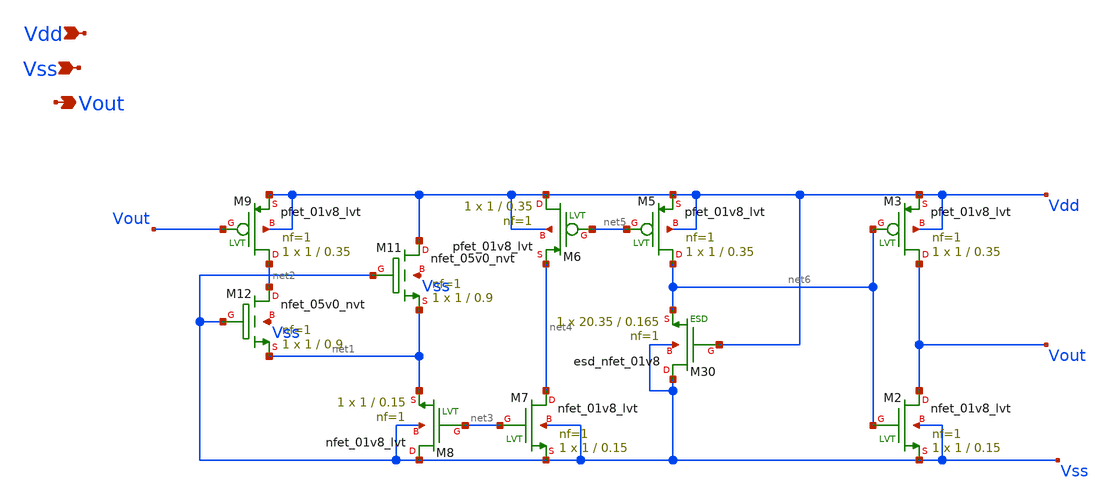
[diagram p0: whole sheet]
** sch_path: tt10-hdl/tt_um_test_commit/xschem/T2/startup/POR/Z_old/native-HengYou_por.sch
**.subckt native-HengYou_por Vdd Vss Vout
*.ipin Vdd
*.ipin Vss
*.opin Vout
XM30 Vss Vdd net6 Vss sky130_fd_pr__esd_nfet_01v8 L=0.165 W=20.35 nf=1 ad='int((nf+1)/2) * W/nf * 0.29'
+ as='int((nf+2)/2) * W/nf * 0.29' pd='2*int((nf+1)/2) * (W/nf + 0.29)' ps='2*int((nf+2)/2) * (W/nf + 0.29)'
+ nrd='0.29 / W' nrs='0.29 / W' sa=0 sb=0 sd=0 mult=1 m=1
XM2 Vout net6 Vss Vss sky130_fd_pr__nfet_01v8_lvt L=0.15 W=1 nf=1 ad='int((1 + 1)/2) * 1 / 1 * 0.29'
+ as='int((1 + 2)/2) * 1 / 1 * 0.29' pd='2*int((1 + 1)/2) * (1 / 1 + 0.29)' ps='2*int((1 + 2)/2) * (1 / 1 + 0.29)'
+ nrd='0.29 / 1 ' nrs='0.29 / 1 ' sa=0 sb=0 sd=0 mult=1 m=1
XM3 Vout net6 Vdd Vdd sky130_fd_pr__pfet_01v8_lvt L=0.35 W=1 nf=1 ad='int((1 + 1)/2) * 1 / 1 * 0.29'
+ as='int((1 + 2)/2) * 1 / 1 * 0.29' pd='2*int((1 + 1)/2) * (1 / 1 + 0.29)' ps='2*int((1 + 2)/2) * (1 / 1 + 0.29)'
+ nrd='0.29 / 1 ' nrs='0.29 / 1 ' sa=0 sb=0 sd=0 mult=1 m=1
XM5 net6 net5 Vdd Vdd sky130_fd_pr__pfet_01v8_lvt L=0.35 W=1 nf=1 ad='int((1 + 1)/2) * 1 / 1 * 0.29'
+ as='int((1 + 2)/2) * 1 / 1 * 0.29' pd='2*int((1 + 1)/2) * (1 / 1 + 0.29)' ps='2*int((1 + 2)/2) * (1 / 1 + 0.29)'
+ nrd='0.29 / 1 ' nrs='0.29 / 1 ' sa=0 sb=0 sd=0 mult=1 m=1
XM6 Vdd net5 net4 Vdd sky130_fd_pr__pfet_01v8_lvt L=0.35 W=1 nf=1 ad='int((1 + 1)/2) * 1 / 1 * 0.29'
+ as='int((1 + 2)/2) * 1 / 1 * 0.29' pd='2*int((1 + 1)/2) * (1 / 1 + 0.29)' ps='2*int((1 + 2)/2) * (1 / 1 + 0.29)'
+ nrd='0.29 / 1 ' nrs='0.29 / 1 ' sa=0 sb=0 sd=0 mult=1 m=1
XM7 net4 net3 Vss Vss sky130_fd_pr__nfet_01v8_lvt L=0.15 W=1 nf=1 ad='int((1 + 1)/2) * 1 / 1 * 0.29'
+ as='int((1 + 2)/2) * 1 / 1 * 0.29' pd='2*int((1 + 1)/2) * (1 / 1 + 0.29)' ps='2*int((1 + 2)/2) * (1 / 1 + 0.29)'
+ nrd='0.29 / 1 ' nrs='0.29 / 1 ' sa=0 sb=0 sd=0 mult=1 m=1
XM8 Vss net3 net1 Vss sky130_fd_pr__nfet_01v8_lvt L=0.15 W=1 nf=1 ad='int((1 + 1)/2) * 1 / 1 * 0.29'
+ as='int((1 + 2)/2) * 1 / 1 * 0.29' pd='2*int((1 + 1)/2) * (1 / 1 + 0.29)' ps='2*int((1 + 2)/2) * (1 / 1 + 0.29)'
+ nrd='0.29 / 1 ' nrs='0.29 / 1 ' sa=0 sb=0 sd=0 mult=1 m=1
XM9 net2 Vout Vdd Vdd sky130_fd_pr__pfet_01v8_lvt L=0.35 W=1 nf=1 ad='int((1 + 1)/2) * 1 / 1 * 0.29'
+ as='int((1 + 2)/2) * 1 / 1 * 0.29' pd='2*int((1 + 1)/2) * (1 / 1 + 0.29)' ps='2*int((1 + 2)/2) * (1 / 1 + 0.29)'
+ nrd='0.29 / 1 ' nrs='0.29 / 1 ' sa=0 sb=0 sd=0 mult=1 m=1
XM11 Vdd Vss net1 Vss sky130_fd_pr__nfet_05v0_nvt L=0.9 W=1 nf=1 ad='int((1 + 1)/2) * 1 / 1 * 0.29' as='int((1 + 2)/2) * 1 / 1 * 0.29'
+ pd='2*int((1 + 1)/2) * (1 / 1 + 0.29)' ps='2*int((1 + 2)/2) * (1 / 1 + 0.29)' nrd='0.29 / 1 ' nrs='0.29 / 1 '
+ sa=0 sb=0 sd=0 mult=1 m=1
XM12 net2 Vss net1 Vss sky130_fd_pr__nfet_05v0_nvt L=0.9 W=1 nf=1 ad='int((1 + 1)/2) * 1 / 1 * 0.29'
+ as='int((1 + 2)/2) * 1 / 1 * 0.29' pd='2*int((1 + 1)/2) * (1 / 1 + 0.29)' ps='2*int((1 + 2)/2) * (1 / 1 + 0.29)'
+ nrd='0.29 / 1 ' nrs='0.29 / 1 ' sa=0 sb=0 sd=0 mult=1 m=1
**.ends
.end
